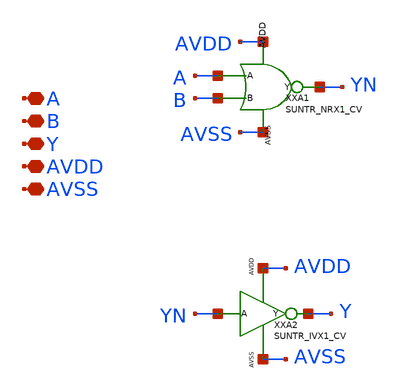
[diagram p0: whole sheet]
** sch_path: design/SUN_TR_SKY130NM/SUNTR_ORX4_CV.sch
**.subckt SUNTR_ORX4_CV A B Y AVDD AVSS
*.iopin A
*.iopin B
*.iopin Y
*.iopin AVDD
*.iopin AVSS
XXA1 A B YN AVDD AVSS SUNTR_NRX1_CV
XXA2 YN Y AVDD AVSS SUNTR_IVX1_CV
**.ends
.end
